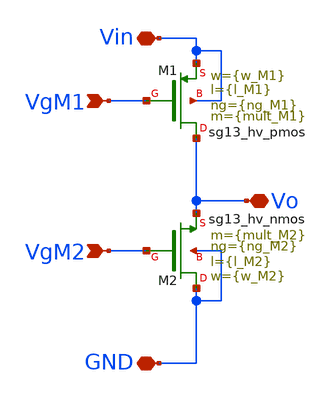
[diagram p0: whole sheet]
** sch_path: xschem/DCDCBuck_vto1p1.sch
**.subckt DCDCBuck_vto1p1 Vin VgM1 VgM2 Vo GND
*.iopin Vin
*.ipin VgM1
*.ipin VgM2
*.iopin Vo
*.iopin GND
XM2 GND VgM2 Vo GND sg13_hv_nmos w={w_M2} l={l_M2} ng={ng_M2} m={mult_M2} mm_ok=1
XM1 Vo VgM1 Vin Vin sg13_hv_pmos w={w_M1} l={l_M1} ng={ng_M1} m={mult_M1} mm_ok=1
**.ends
.end
